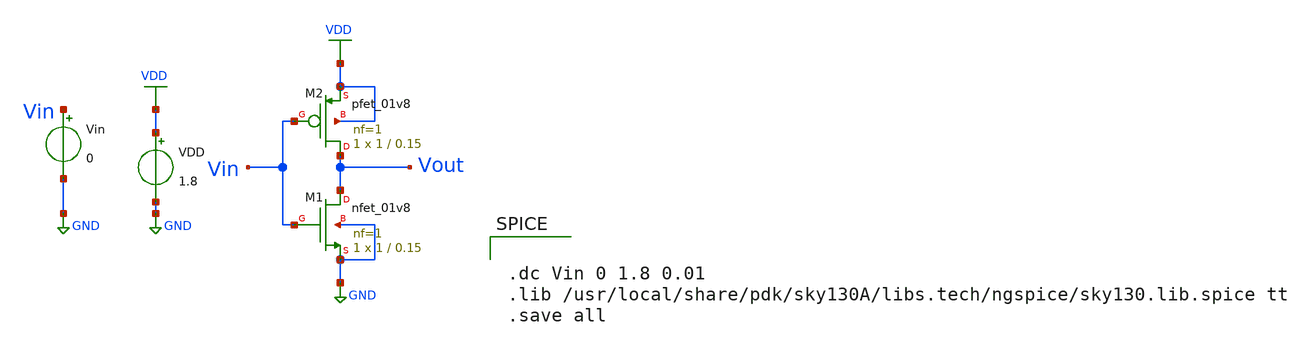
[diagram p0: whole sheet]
** sch_path: week1/designs/xschem/pre-layout/inverter.sch
**.subckt inverter
XM1 Vout Vin GND GND sky130_fd_pr__nfet_01v8 L=0.15 W=1 nf=1 ad='int((nf+1)/2) * W/nf * 0.29' as='int((nf+2)/2) * W/nf * 0.29'
+ pd='2*int((nf+1)/2) * (W/nf + 0.29)' ps='2*int((nf+2)/2) * (W/nf + 0.29)' nrd='0.29 / W' nrs='0.29 / W'
+ sa=0 sb=0 sd=0 mult=1 m=1
XM2 Vout Vin VDD VDD sky130_fd_pr__pfet_01v8 L=0.15 W=1 nf=1 ad='int((nf+1)/2) * W/nf * 0.29' as='int((nf+2)/2) * W/nf * 0.29'
+ pd='2*int((nf+1)/2) * (W/nf + 0.29)' ps='2*int((nf+2)/2) * (W/nf + 0.29)' nrd='0.29 / W' nrs='0.29 / W'
+ sa=0 sb=0 sd=0 mult=1 m=1
VDD VDD GND 1.8
Vin Vin GND 0
**** begin user architecture code


.dc Vin 0 1.8 0.01
.lib /usr/local/share/pdk/sky130A/libs.tech/ngspice/sky130.lib.spice tt
.save all

**** end user architecture code
**.ends
.GLOBAL GND
.GLOBAL VDD
.end
